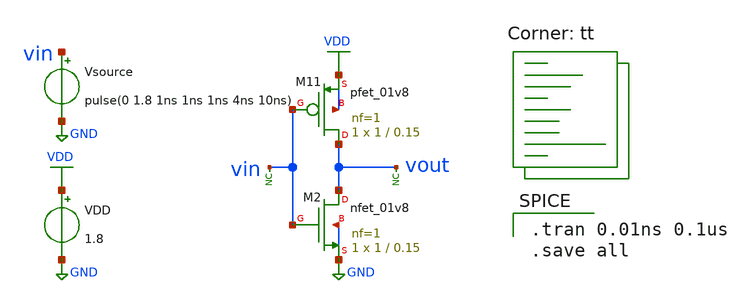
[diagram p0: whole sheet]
** sch_path: pll/lc_vco_lib/Ahmed Elshahat LC VCO/inverter_demo/inverter_demo.sch
**.subckt inverter_demo
XM11 vout vin VDD VDD sky130_fd_pr__pfet_01v8 L=0.15 W=1 nf=1 ad='int((nf+1)/2) * W/nf * 0.29' as='int((nf+2)/2) * W/nf * 0.29'
+ pd='2*int((nf+1)/2) * (W/nf + 0.29)' ps='2*int((nf+2)/2) * (W/nf + 0.29)' nrd='0.29 / W' nrs='0.29 / W'
+ sa=0 sb=0 sd=0 mult=1 m=1
XM2 vout vin GND GND sky130_fd_pr__nfet_01v8 L=0.15 W=1 nf=1 ad='int((1 + 1)/2) * 1 / 1 * 0.29' as='int((1 + 2)/2) * 1 / 1 * 0.29'
+ pd='2*int((1 + 1)/2) * (1 / 1 + 0.29)' ps='2*int((1 + 2)/2) * (1 / 1 + 0.29)' nrd='0.29 / 1 ' nrs='0.29 / 1 '
+ sa=0 sb=0 sd=0 mult=1 m=1
VDD VDD GND 1.8
Vsource vin GND pulse(0 1.8 1ns 1ns 1ns 4ns 10ns)
* noconn vout
* noconn vin
**** begin user architecture code

.tran 0.01ns 0.1us
.save all

.lib $::SKYWATER_MODELS/sky130.lib.spice tt
**** end user architecture code
**.ends
.GLOBAL VDD
.GLOBAL GND
.end
